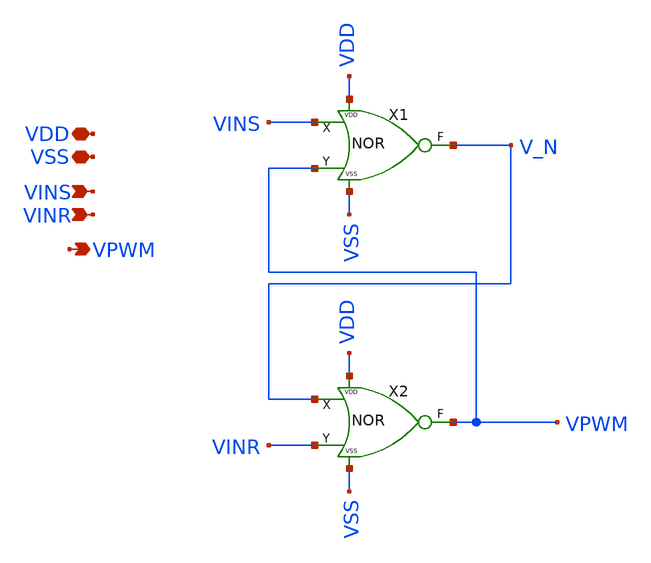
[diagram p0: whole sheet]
** sch_path: xschem/SR_Latch_NOR/SR_Latch.sch
**.subckt SR_Latch VDD VINS VSS VPWM VINR
*.iopin VDD
*.ipin VINS
*.iopin VSS
*.opin VPWM
*.ipin VINR
X1 VDD VSS V_N VINS VPWM NOR
X2 VDD VSS VPWM V_N VINR NOR
**** begin user architecture code



**** end user architecture code
**.ends

* expanding   symbol:  ../DigitalGates/NOR.sym # of pins=5
** sym_path: xschem/DigitalGates/NOR.sym
** sch_path: xschem/DigitalGates/NOR.sch
.subckt NOR VDD VSS F X Y
*.iopin VDD
*.ipin X
*.opin F
*.iopin VSS
*.ipin Y
XM4 F Y net1 VDD sg13_lv_pmos w=0.15u l=0.13u ng=1 m=6 mm_ok=1
XM3 F X VSS VSS sg13_lv_nmos w=0.15u l=0.13u ng=1 m=1 mm_ok=1
XM1 F Y VSS VSS sg13_lv_nmos w=0.15u l=0.13u ng=1 m=1 mm_ok=1
XM2 net1 X VDD VDD sg13_lv_pmos w=0.15u l=0.13u ng=1 m=6 mm_ok=1
**** begin user architecture code



**** end user architecture code
.ends

.end
